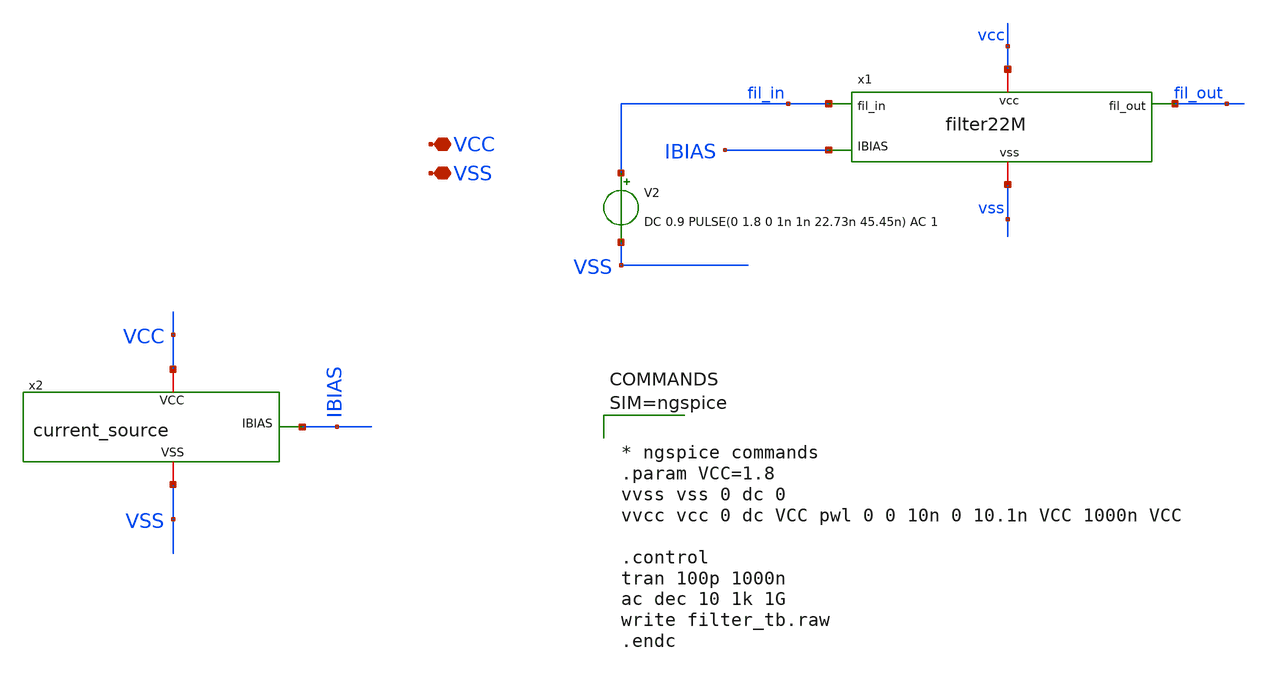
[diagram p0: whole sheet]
** sch_path: xschem/filter22M_TB.sch
**.subckt filter22M_TB VCC VSS
*.iopin VCC
*.iopin VSS
x1 vcc fil_out fil_in vss IBIAS filter22M
V2 fil_in VSS DC 0.9 PULSE(0 1.8 0 1n 1n 22.73n 45.45n) AC 1
x2 VCC VSS IBIAS current_source
**** begin user architecture code

** opencircuitdesign pdks install
.lib $::SKYWATER_MODELS/sky130.lib.spice tt





* ngspice commands
.param VCC=1.8
vvss vss 0 dc 0
vvcc vcc 0 dc VCC pwl 0 0 10n 0 10.1n VCC 1000n VCC

.control
tran 100p 1000n
ac dec 10 1k 1G
write filter_tb.raw
.endc




**** end user architecture code
**.ends

* expanding   symbol:  filter22M.sym # of pins=5
** sym_path: xschem/filter22M.sym
** sch_path: xschem/filter22M.sch
.subckt filter22M vcc fil_out fil_in vss IBIAS
*.opin fil_out
*.ipin fil_in
*.iopin vcc
*.iopin vss
*.ipin IBIAS
x1 VCC fil_out fil_out net1 VSS IBIAS opamp_1
XR1 fil_in mid sky130_fd_pr__res_generic_po W=0.5 L=100 m=1
XR2 mid net1 sky130_fd_pr__res_generic_po W=0.5 L=100 m=1
XC1 mid fil_out sky130_fd_pr__cap_mim_m3_2 W=10 L=12 MF=4 m=4
XC2 net1 VSS sky130_fd_pr__cap_mim_m3_2 W=10 L=6 MF=4 m=4
.ends


* expanding   symbol:  current_source.sym # of pins=3
** sym_path: xschem/current_source.sym
** sch_path: xschem/current_source.sch
.subckt current_source VCC VSS IBIAS
*.iopin VCC
*.iopin VSS
*.opin IBIAS
XM3 IBIAS IBIAS VSS VSS sky130_fd_pr__nfet_01v8 L=1 W=40 nf=1 ad='int((nf+1)/2) * W/nf * 0.29' as='int((nf+2)/2) * W/nf * 0.29'
+ pd='2*int((nf+1)/2) * (W/nf + 0.29)' ps='2*int((nf+2)/2) * (W/nf + 0.29)' nrd='0.29 / W' nrs='0.29 / W'
+ sa=0 sb=0 sd=0 mult=1 m=1
XR1 IBIAS VCC sky130_fd_pr__res_generic_po W=0.33 L=12 m=1
.ends


* expanding   symbol:  opamp_1.sym # of pins=6
** sym_path: xschem/opamp_1.sym
** sch_path: xschem/opamp_1.sch
.subckt opamp_1 VCC OUT INA INB VSS IBIAS
*.ipin INA
*.ipin INB
*.opin OUT
*.iopin VCC
*.iopin VSS
*.ipin IBIAS
XM1 MIRR INA TAILV VSS sky130_fd_pr__nfet_01v8 L=1 W=20 nf=1 ad='int((nf+1)/2) * W/nf * 0.29' as='int((nf+2)/2) * W/nf * 0.29'
+ pd='2*int((nf+1)/2) * (W/nf + 0.29)' ps='2*int((nf+2)/2) * (W/nf + 0.29)' nrd='0.29 / W' nrs='0.29 / W'
+ sa=0 sb=0 sd=0 mult=1 m=1
XM2 DIFF_OUT INB TAILV VSS sky130_fd_pr__nfet_01v8 L=1 W=20 nf=1 ad='int((nf+1)/2) * W/nf * 0.29' as='int((nf+2)/2) * W/nf * 0.29'
+ pd='2*int((nf+1)/2) * (W/nf + 0.29)' ps='2*int((nf+2)/2) * (W/nf + 0.29)' nrd='0.29 / W' nrs='0.29 / W'
+ sa=0 sb=0 sd=0 mult=1 m=1
XM3 TAILV IBIAS VSS VSS sky130_fd_pr__nfet_01v8 L=1 W=40 nf=1 ad='int((nf+1)/2) * W/nf * 0.29' as='int((nf+2)/2) * W/nf * 0.29'
+ pd='2*int((nf+1)/2) * (W/nf + 0.29)' ps='2*int((nf+2)/2) * (W/nf + 0.29)' nrd='0.29 / W' nrs='0.29 / W'
+ sa=0 sb=0 sd=0 mult=1 m=1
XM4 MIRR MIRR VCC VCC sky130_fd_pr__pfet_01v8_lvt L=0.5 W=14 nf=1 ad='int((nf+1)/2) * W/nf * 0.29' as='int((nf+2)/2) * W/nf * 0.29'
+ pd='2*int((nf+1)/2) * (W/nf + 0.29)' ps='2*int((nf+2)/2) * (W/nf + 0.29)' nrd='0.29 / W' nrs='0.29 / W'
+ sa=0 sb=0 sd=0 mult=1 m=1
XM5 DIFF_OUT MIRR VCC VCC sky130_fd_pr__pfet_01v8_lvt L=0.5 W=14 nf=1 ad='int((nf+1)/2) * W/nf * 0.29'
+ as='int((nf+2)/2) * W/nf * 0.29' pd='2*int((nf+1)/2) * (W/nf + 0.29)' ps='2*int((nf+2)/2) * (W/nf + 0.29)'
+ nrd='0.29 / W' nrs='0.29 / W' sa=0 sb=0 sd=0 mult=1 m=1
XM6 OUT IBIAS VSS VSS sky130_fd_pr__nfet_01v8 L=0.5 W=93 nf=1 ad='int((nf+1)/2) * W/nf * 0.29' as='int((nf+2)/2) * W/nf * 0.29'
+ pd='2*int((nf+1)/2) * (W/nf + 0.29)' ps='2*int((nf+2)/2) * (W/nf + 0.29)' nrd='0.29 / W' nrs='0.29 / W'
+ sa=0 sb=0 sd=0 mult=1 m=1
XM7 OUT DIFF_OUT VCC VCC sky130_fd_pr__pfet_01v8_lvt L=0.5 W=70 nf=1 ad='int((nf+1)/2) * W/nf * 0.29'
+ as='int((nf+2)/2) * W/nf * 0.29' pd='2*int((nf+1)/2) * (W/nf + 0.29)' ps='2*int((nf+2)/2) * (W/nf + 0.29)'
+ nrd='0.29 / W' nrs='0.29 / W' sa=0 sb=0 sd=0 mult=1 m=1
XM9 RBIAS IBIAS VSS VSS sky130_fd_pr__nfet_01v8 L=1 W=5 nf=1 ad='int((nf+1)/2) * W/nf * 0.29' as='int((nf+2)/2) * W/nf * 0.29'
+ pd='2*int((nf+1)/2) * (W/nf + 0.29)' ps='2*int((nf+2)/2) * (W/nf + 0.29)' nrd='0.29 / W' nrs='0.29 / W'
+ sa=0 sb=0 sd=0 mult=1 m=1
XM10 RBIAS RBIAS net2 VCC sky130_fd_pr__pfet_01v8_lvt L=0.5 W=1 nf=1 ad='int((nf+1)/2) * W/nf * 0.29'
+ as='int((nf+2)/2) * W/nf * 0.29' pd='2*int((nf+1)/2) * (W/nf + 0.29)' ps='2*int((nf+2)/2) * (W/nf + 0.29)'
+ nrd='0.29 / W' nrs='0.29 / W' sa=0 sb=0 sd=0 mult=1 m=1
XM11 net2 net2 VCC VCC sky130_fd_pr__pfet_01v8_lvt L=0.5 W=7.5 nf=1 ad='int((nf+1)/2) * W/nf * 0.29'
+ as='int((nf+2)/2) * W/nf * 0.29' pd='2*int((nf+1)/2) * (W/nf + 0.29)' ps='2*int((nf+2)/2) * (W/nf + 0.29)'
+ nrd='0.29 / W' nrs='0.29 / W' sa=0 sb=0 sd=0 mult=1 m=1
XC1 OUT net1 sky130_fd_pr__cap_mim_m3_2 W=20 L=13 MF=1 m=1
XM8 net1 RBIAS DIFF_OUT VCC sky130_fd_pr__pfet_01v8_lvt L=0.5 W=14 nf=1 ad='int((nf+1)/2) * W/nf * 0.29'
+ as='int((nf+2)/2) * W/nf * 0.29' pd='2*int((nf+1)/2) * (W/nf + 0.29)' ps='2*int((nf+2)/2) * (W/nf + 0.29)'
+ nrd='0.29 / W' nrs='0.29 / W' sa=0 sb=0 sd=0 mult=1 m=1
.ends

.end
